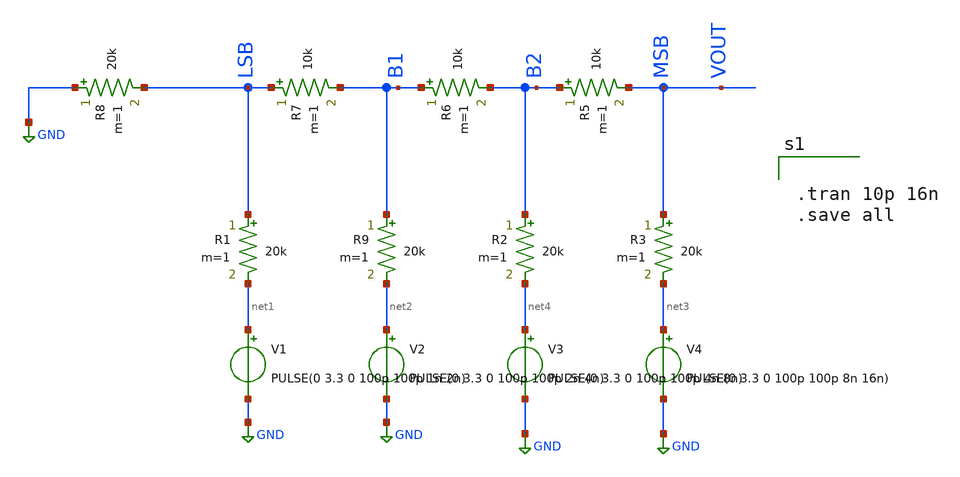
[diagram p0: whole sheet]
** sch_path: xschem/R2R_DAC.sch
**.subckt R2R_DAC
R1 LSB net1 20k m=1
R5 B2 VOUT 10k m=1
R6 B1 B2 10k m=1
R7 LSB B1 10k m=1
R8 GND LSB 20k m=1
R9 B1 net2 20k m=1
R2 B2 net4 20k m=1
R3 VOUT net3 20k m=1
V2 net2 GND PULSE(0 3.3 0 100p 100p 2n 4n)
V3 net4 GND PULSE(0 3.3 0 100p 100p 4n 8n)
V1 net1 GND PULSE(0 3.3 0 100p 100p 1n 2n)
V4 net3 GND PULSE(0 3.3 0 100p 100p 8n 16n)
**** begin user architecture code


.tran 10p 16n
.save all


**** end user architecture code
**.ends
.GLOBAL GND
.end
